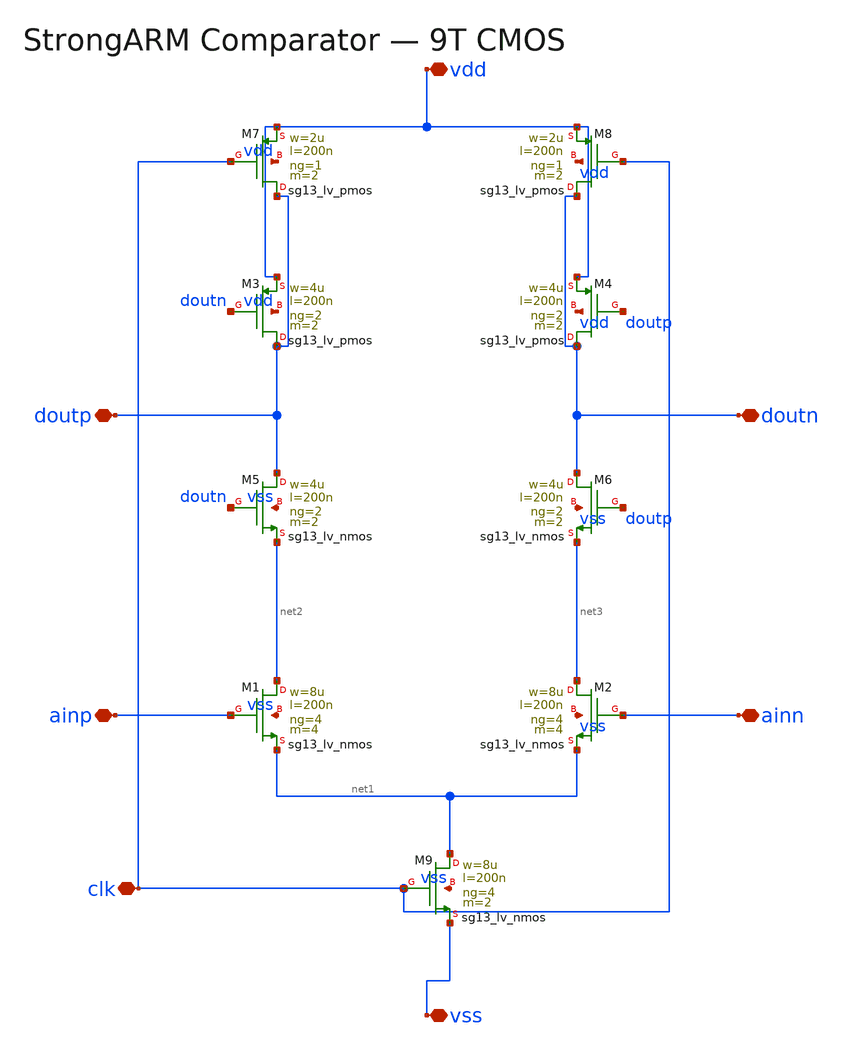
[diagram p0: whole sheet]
** sch_path: xschem/blocks/ADC_SAR_12B.sch
**.subckt ADC_SAR_12B ainp ainn clk doutp doutn vdd vss
*.iopin ainp
*.iopin ainn
*.iopin clk
*.iopin doutp
*.iopin doutn
*.iopin vdd
*.iopin vss
XM1 net2 ainp net1 vss sg13_lv_nmos w=8u l=200n ng=4 m=4 mm_ok=1
XM2 net3 ainn net1 vss sg13_lv_nmos w=8u l=200n ng=4 m=4 mm_ok=1
XM9 net1 clk vss vss sg13_lv_nmos w=8u l=200n ng=4 m=2 mm_ok=1
XM5 doutp doutn net2 vss sg13_lv_nmos w=4u l=200n ng=2 m=2 mm_ok=1
XM6 doutn doutp net3 vss sg13_lv_nmos w=4u l=200n ng=2 m=2 mm_ok=1
XM3 doutp doutn vdd vdd sg13_lv_pmos w=4u l=200n ng=2 m=2 mm_ok=1
XM4 doutn doutp vdd vdd sg13_lv_pmos w=4u l=200n ng=2 m=2 mm_ok=1
XM7 doutp clk vdd vdd sg13_lv_pmos w=2u l=200n ng=1 m=2 mm_ok=1
XM8 doutn clk vdd vdd sg13_lv_pmos w=2u l=200n ng=1 m=2 mm_ok=1
**.ends
.end
